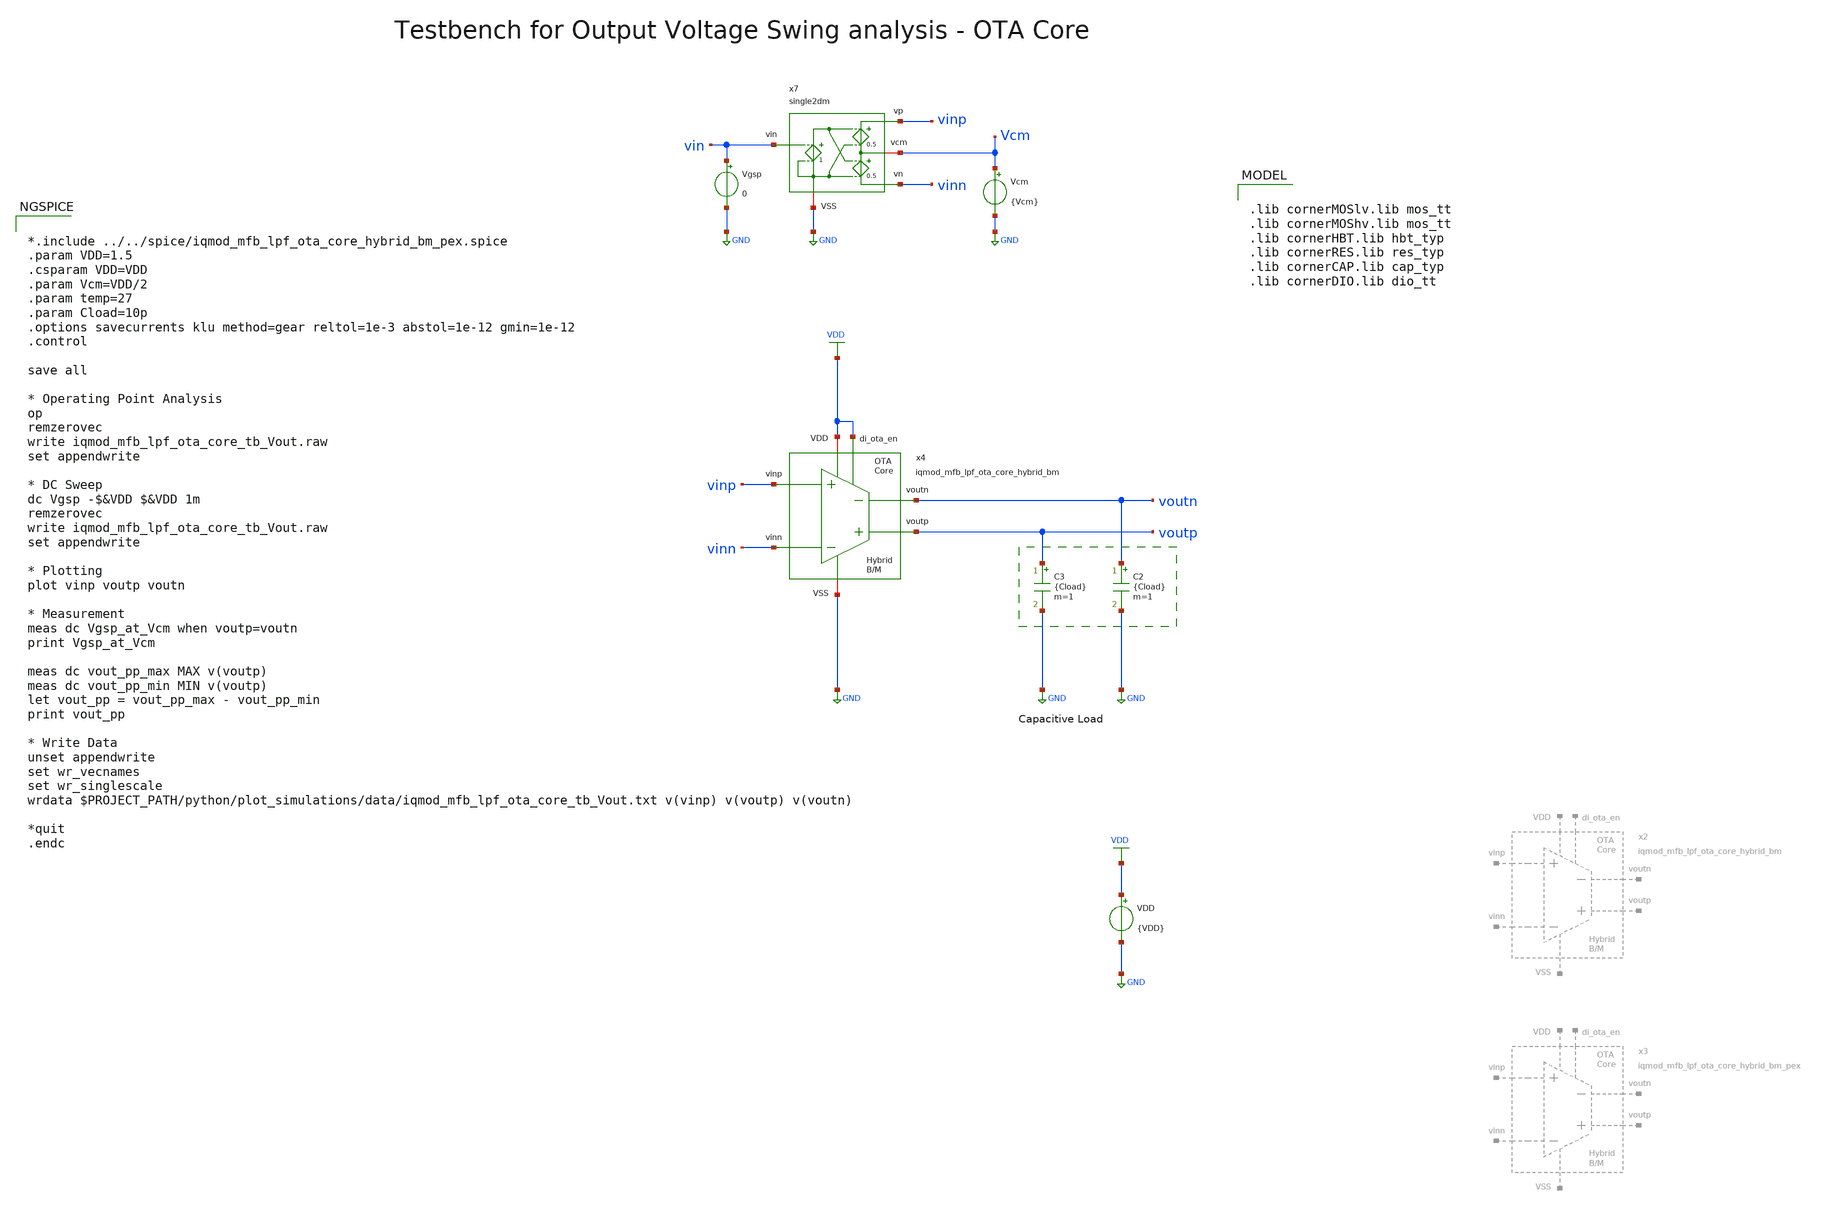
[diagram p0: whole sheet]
** sch_path: ihp130/macros/iqmod/xschem/testbenches/iqmod_mfb_lpf_ota_core_tb_Vout.sch
**.subckt iqmod_mfb_lpf_ota_core_tb_Vout
VDD VDD GND {VDD}
Vgsp vin GND 0
C2 voutn GND {Cload} m=1
C3 voutp GND {Cload} m=1
Vcm Vcm GND {Vcm}
x4 voutp voutn vinn vinp VDD GND VDD iqmod_mfb_lpf_ota_core_hybrid_bm
x7 vinp vin Vcm GND vinn single2dm
**** begin user architecture code


*.include ../../spice/iqmod_mfb_lpf_ota_core_hybrid_bm_pex.spice
.param VDD=1.5
.csparam VDD=VDD
.param Vcm=VDD/2
.param temp=27
.param Cload=10p
.options savecurrents klu method=gear reltol=1e-3 abstol=1e-12 gmin=1e-12
.control

save all

* Operating Point Analysis
op
remzerovec
write iqmod_mfb_lpf_ota_core_tb_Vout.raw
set appendwrite

* DC Sweep
dc Vgsp -$&VDD $&VDD 1m
remzerovec
write iqmod_mfb_lpf_ota_core_tb_Vout.raw
set appendwrite

* Plotting
plot vinp voutp voutn

* Measurement
meas dc Vgsp_at_Vcm when voutp=voutn
print Vgsp_at_Vcm

meas dc vout_pp_max MAX v(voutp)
meas dc vout_pp_min MIN v(voutp)
let vout_pp = vout_pp_max - vout_pp_min
print vout_pp

* Write Data
unset appendwrite
set wr_vecnames
set wr_singlescale
wrdata $PROJECT_PATH/python/plot_simulations/data/iqmod_mfb_lpf_ota_core_tb_Vout.txt v(vinp)
+ v(voutp) v(voutn)

*quit
.endc



.lib cornerMOSlv.lib mos_tt
.lib cornerMOShv.lib mos_tt
.lib cornerHBT.lib hbt_typ
.lib cornerRES.lib res_typ
.lib cornerCAP.lib cap_typ
.lib cornerDIO.lib dio_tt

**** end user architecture code
**.ends
.GLOBAL GND
.GLOBAL VDD
.end
